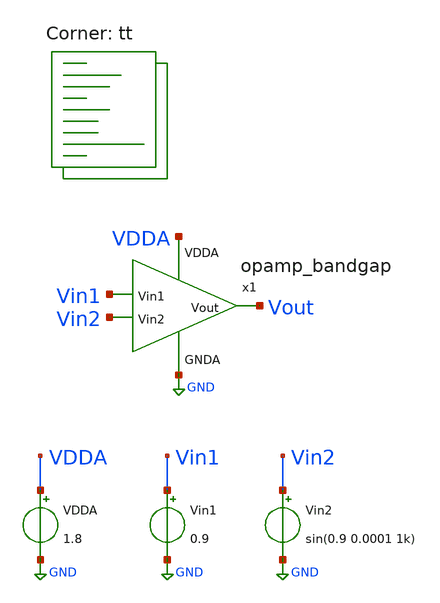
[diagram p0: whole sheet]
** sch_path: projects/pll/bandgapref/xschem_ngspice/tb_opamp_bandgap.sch
**.subckt tb_opamp_bandgap
VDDA VDDA GND 1.8
Vin1 Vin1 GND 0.9
Vin2 Vin2 GND sin(0.9 0.0001 1k)
x1 VDDA Vout Vin2 Vin1 GND opamp_bandgap
**** begin user architecture code



.option wnflag=1

* .param VDDGAUSS = agauss(1.8, 0.05, 1)
* .param VDD = VDDGAUSS
* .param VDD = 1.8

* .param TEMPGAUSS = agauss(40, 30, 1)
* .param temp = TEMPGAUSS
.option temp = 26

.control

  save all
  tran 1u 20m
  * ac dec 20 1 1T

  write tb_opamp_bandgap.raw
  set appendwrite

.endc



.lib $::SKYWATER_MODELS/sky130.lib.spice tt
**** end user architecture code
**.ends

* expanding   symbol:
*+  /foss/designs/my_design/projects/pll/bandgapref/xschem_ngspice/opamp_bandgap.sym # of pins=5
** sym_path: projects/pll/bandgapref/xschem_ngspice/opamp_bandgap.sym
** sch_path: projects/pll/bandgapref/xschem_ngspice/opamp_bandgap.sch
.subckt opamp_bandgap VDDA Vout Vin2 Vin1 GNDA
*.ipin Vin1
*.opin Vout
*.ipin Vin2
*.ipin GNDA
*.ipin VDDA
XM2 net1 Vin1 net2 GNDA sky130_fd_pr__nfet_01v8 L=0.15 W=1 nf=1 ad='int((nf+1)/2) * W/nf * 0.29' as='int((nf+2)/2) * W/nf * 0.29'
+ pd='2*int((nf+1)/2) * (W/nf + 0.29)' ps='2*int((nf+2)/2) * (W/nf + 0.29)' nrd='0.29 / W' nrs='0.29 / W'
+ sa=0 sb=0 sd=0 mult=1 m=1
XM3 Vout Vin2 net2 GNDA sky130_fd_pr__nfet_01v8 L=0.15 W=1 nf=1 ad='int((nf+1)/2) * W/nf * 0.29' as='int((nf+2)/2) * W/nf * 0.29'
+ pd='2*int((nf+1)/2) * (W/nf + 0.29)' ps='2*int((nf+2)/2) * (W/nf + 0.29)' nrd='0.29 / W' nrs='0.29 / W'
+ sa=0 sb=0 sd=0 mult=1 m=1
XM4 net1 net1 VDDA VDDA sky130_fd_pr__pfet_01v8 L=0.15 W=2 nf=1 ad='int((nf+1)/2) * W/nf * 0.29' as='int((nf+2)/2) * W/nf * 0.29'
+ pd='2*int((nf+1)/2) * (W/nf + 0.29)' ps='2*int((nf+2)/2) * (W/nf + 0.29)' nrd='0.29 / W' nrs='0.29 / W'
+ sa=0 sb=0 sd=0 mult=1 m=1
XM5 Vout net1 VDDA VDDA sky130_fd_pr__pfet_01v8 L=0.15 W=2 nf=1 ad='int((nf+1)/2) * W/nf * 0.29' as='int((nf+2)/2) * W/nf * 0.29'
+ pd='2*int((nf+1)/2) * (W/nf + 0.29)' ps='2*int((nf+2)/2) * (W/nf + 0.29)' nrd='0.29 / W' nrs='0.29 / W'
+ sa=0 sb=0 sd=0 mult=1 m=1
XM1 net2 net2 GNDA GNDA sky130_fd_pr__nfet_01v8 L=0.15 W=1 nf=1 ad='int((nf+1)/2) * W/nf * 0.29' as='int((nf+2)/2) * W/nf * 0.29'
+ pd='2*int((nf+1)/2) * (W/nf + 0.29)' ps='2*int((nf+2)/2) * (W/nf + 0.29)' nrd='0.29 / W' nrs='0.29 / W'
+ sa=0 sb=0 sd=0 mult=1 m=1
.ends

.GLOBAL GND
.end
